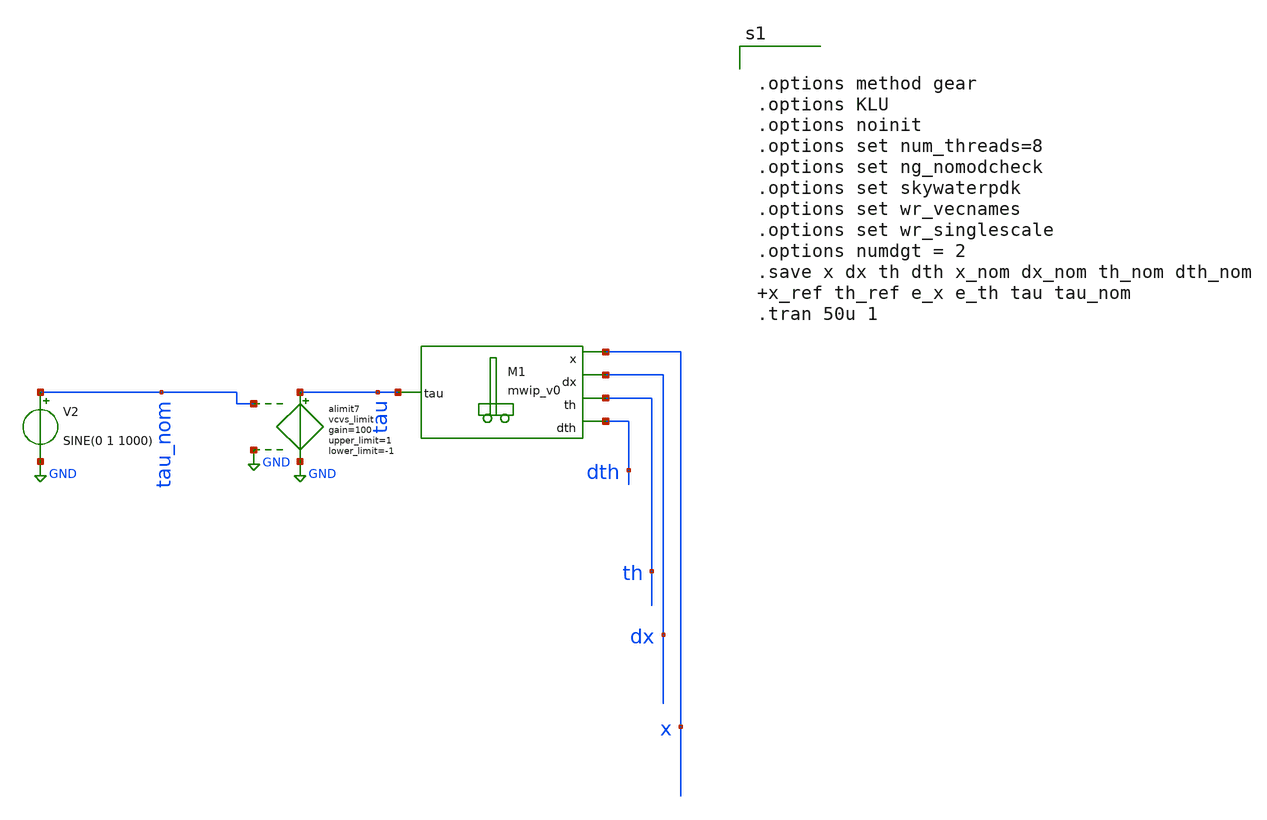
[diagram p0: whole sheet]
** sch_path: tb_mwip.sch
**.subckt tb_mwip
XM1 x dx th dth tau mwip_v0
alimit7 %vd( tau_nom GND ) %vd( tau GND ) alimit7
.model alimit7 limit ( gain=100 out_lower_limit=-1 out_upper_limit=1 )
V2 tau_nom GND SINE(0 1 1000)
**** begin user architecture code

*MADE BY JORGE ALEJANDRO JUAREZ LORA IPN


.subckt mwip_v0 Tau X Th vx vTh
    N1 Tau X Th vx vTh  mwip_v0_model init_x=0 init_theta=0.1
.ends mwip_v0

.model mwip_v0_model mwip_dynamics

.control
    pre_osdi /foss/designs/SNN-MWIP/Memristor/rram_v0.osdi
    pre_osdi /foss/designs/SNN-MWIP/MWIP/mwip.osdi
.endc



.options method gear
.options KLU
.options noinit
.options set num_threads=8
.options set ng_nomodcheck
.options set skywaterpdk
.options set wr_vecnames
.options set wr_singlescale
.options numdgt = 2
.save x dx th dth x_nom dx_nom th_nom dth_nom x_ref th_ref e_x e_th tau tau_nom
.tran 50u 1



**** end user architecture code
**.ends
.GLOBAL GND
.end
